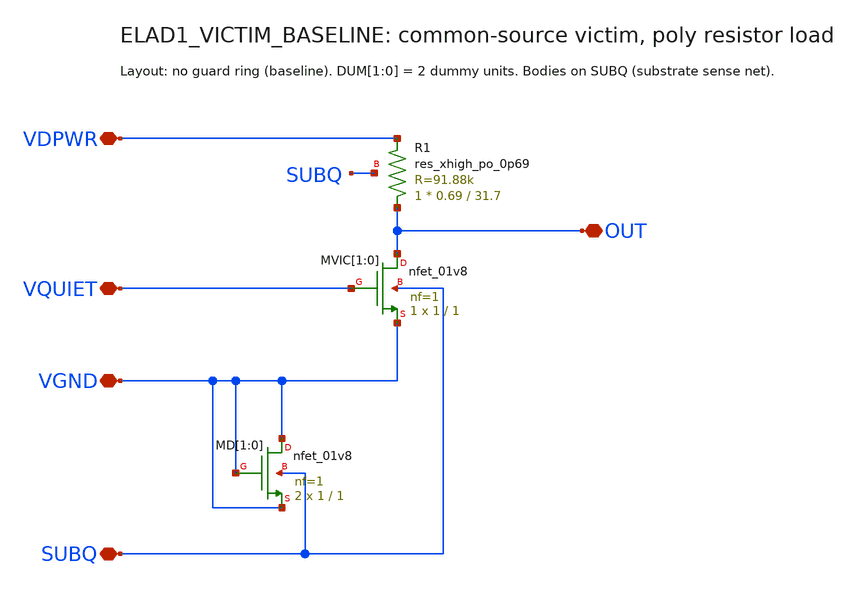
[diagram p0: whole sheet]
** sch_path: cells/ELAD1_VICTIM_BASELINE/schematic/ELAD1_VICTIM_BASELINE.sch
**.subckt ELAD1_VICTIM_BASELINE VQUIET OUT VDPWR VGND SUBQ
*.iopin VQUIET
*.iopin OUT
*.iopin VDPWR
*.iopin VGND
*.iopin SUBQ
XMVIC[1] OUT VQUIET VGND SUBQ sky130_fd_pr__nfet_01v8 L=1 W=1 nf=1 ad='int((1 + 1)/2) * 1 / 1 * 0.29'
+ as='int((1 + 2)/2) * 1 / 1 * 0.29' pd='2*int((1 + 1)/2) * (1 / 1 + 0.29)' ps='2*int((1 + 2)/2) * (1 / 1 + 0.29)'
+ nrd='0.29 / 1 ' nrs='0.29 / 1 ' sa=0 sb=0 sd=0 mult=1 m=1
XMVIC[0] OUT VQUIET VGND SUBQ sky130_fd_pr__nfet_01v8 L=1 W=1 nf=1 ad='int((1 + 1)/2) * 1 / 1 * 0.29'
+ as='int((1 + 2)/2) * 1 / 1 * 0.29' pd='2*int((1 + 1)/2) * (1 / 1 + 0.29)' ps='2*int((1 + 2)/2) * (1 / 1 + 0.29)'
+ nrd='0.29 / 1 ' nrs='0.29 / 1 ' sa=0 sb=0 sd=0 mult=1 m=1
XMD[1] VGND VGND VGND SUBQ sky130_fd_pr__nfet_01v8 L=1 W=1 nf=1 ad='int((1 + 1)/2) * 1 / 1 * 0.29' as='int((1 + 2)/2) * 1 / 1 * 0.29'
+ pd='2*int((1 + 1)/2) * (1 / 1 + 0.29)' ps='2*int((1 + 2)/2) * (1 / 1 + 0.29)' nrd='0.29 / 1 ' nrs='0.29 / 1 '
+ sa=0 sb=0 sd=0 mult=2 m=2
XMD[0] VGND VGND VGND SUBQ sky130_fd_pr__nfet_01v8 L=1 W=1 nf=1 ad='int((1 + 1)/2) * 1 / 1 * 0.29' as='int((1 + 2)/2) * 1 / 1 * 0.29'
+ pd='2*int((1 + 1)/2) * (1 / 1 + 0.29)' ps='2*int((1 + 2)/2) * (1 / 1 + 0.29)' nrd='0.29 / 1 ' nrs='0.29 / 1 '
+ sa=0 sb=0 sd=0 mult=2 m=2
XR1 OUT VDPWR SUBQ sky130_fd_pr__res_xhigh_po_0p69 L=31.7 mult=1 m=1
**.ends
.end
